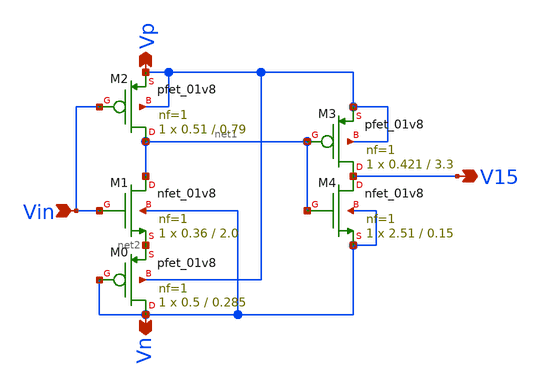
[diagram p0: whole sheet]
** sch_path: xschem/Vth_sch/Symbol/th15.sch
**.subckt th15 Vn Vp Vin V15
*.opin Vn
*.opin Vp
*.ipin Vin
*.opin V15
XM3 V15 net1 Vp Vp sky130_fd_pr__pfet_01v8 L=3.3 W=0.421 nf=1 ad='int((nf+1)/2) * W/nf * 0.29' as='int((nf+2)/2) * W/nf * 0.29'
+ pd='2*int((nf+1)/2) * (W/nf + 0.29)' ps='2*int((nf+2)/2) * (W/nf + 0.29)' nrd='0.29 / W' nrs='0.29 / W'
+ sa=0 sb=0 sd=0 mult=1 m=1
XM4 V15 net1 Vn Vn sky130_fd_pr__nfet_01v8 L=0.15 W=2.51 nf=1 ad='int((nf+1)/2) * W/nf * 0.29' as='int((nf+2)/2) * W/nf * 0.29'
+ pd='2*int((nf+1)/2) * (W/nf + 0.29)' ps='2*int((nf+2)/2) * (W/nf + 0.29)' nrd='0.29 / W' nrs='0.29 / W'
+ sa=0 sb=0 sd=0 mult=1 m=1
XM2 net1 Vin Vp Vp sky130_fd_pr__pfet_01v8 L=0.79 W=0.51 nf=1 ad='int((nf+1)/2) * W/nf * 0.29' as='int((nf+2)/2) * W/nf * 0.29'
+ pd='2*int((nf+1)/2) * (W/nf + 0.29)' ps='2*int((nf+2)/2) * (W/nf + 0.29)' nrd='0.29 / W' nrs='0.29 / W'
+ sa=0 sb=0 sd=0 mult=1 m=1
XM1 net1 Vin net2 Vn sky130_fd_pr__nfet_01v8 L=2.0 W=0.36 nf=1 ad='int((nf+1)/2) * W/nf * 0.29' as='int((nf+2)/2) * W/nf * 0.29'
+ pd='2*int((nf+1)/2) * (W/nf + 0.29)' ps='2*int((nf+2)/2) * (W/nf + 0.29)' nrd='0.29 / W' nrs='0.29 / W'
+ sa=0 sb=0 sd=0 mult=1 m=1
XM0 Vn Vn net2 Vp sky130_fd_pr__pfet_01v8 L=0.285 W=0.5 nf=1 ad='int((nf+1)/2) * W/nf * 0.29' as='int((nf+2)/2) * W/nf * 0.29'
+ pd='2*int((nf+1)/2) * (W/nf + 0.29)' ps='2*int((nf+2)/2) * (W/nf + 0.29)' nrd='0.29 / W' nrs='0.29 / W'
+ sa=0 sb=0 sd=0 mult=1 m=1
**.ends
.end
